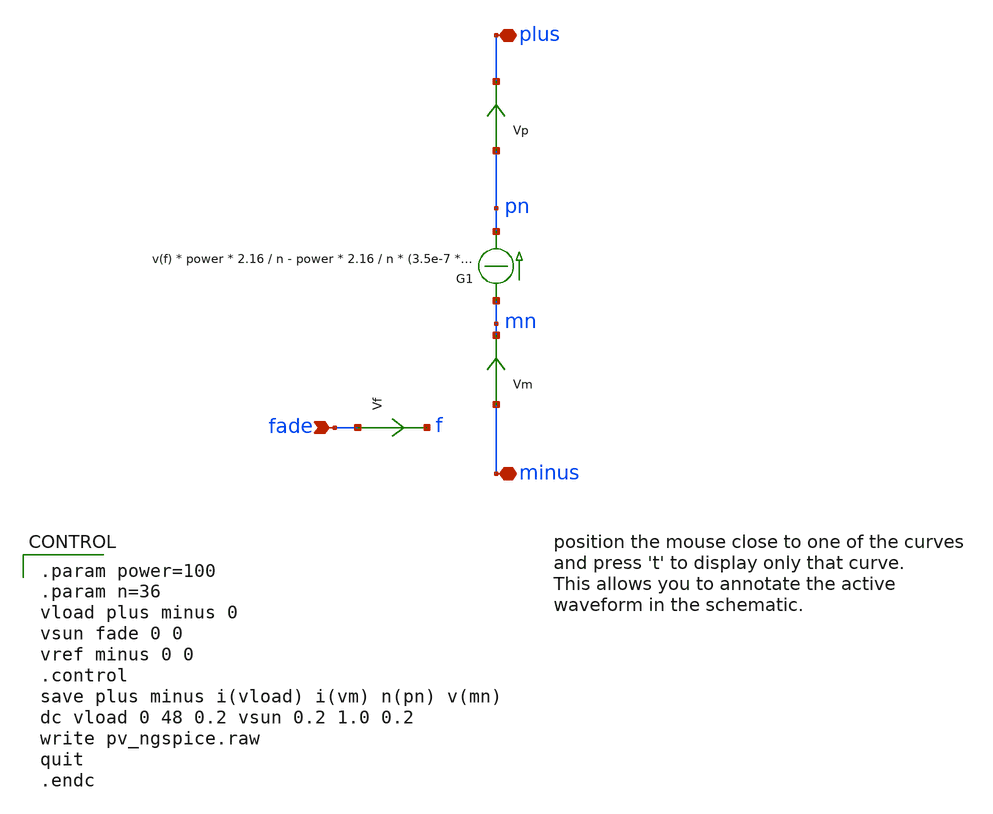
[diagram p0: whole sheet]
** sch_path: xschem_library/ngspice/pv_ngspice.sch
* Copyright (C) 1998-2023 Stefan Frederik Schippers
* This program is free software; you can redistribute it and/or modify
* it under the terms of the GNU General Public License as published by
* the Free Software Foundation; either version 2 of the License, or
* (at your option) any later version.
* This program is distributed in the hope that it will be useful,
* but WITHOUT ANY WARRANTY; without even the implied warranty of
* MERCHANTABILITY or FITNESS FOR A PARTICULAR PURPOSE.  See the
* GNU General Public License for more details.
* You should have received a copy of the GNU General Public License
* along with this program; if not, write to the Free Software
**.subckt pv_ngspice plus minus fade
*.iopin plus
*.iopin minus
*.ipin fade
Vm minus mn 0
.save i(vm)
G1 mn pn CUR=' v(f) * power * 2.16 / n - power * 2.16 / n * (3.5e-7 * exp( v(pn,mn) / n / 0.041)) '
Vf fade f 0
.save i(vf)
Vp pn plus 0
.save i(vp)
**** begin user architecture code

.param power=100
.param n=36
vload plus minus 0
vsun fade 0 0
vref minus 0 0
.control
save plus minus i(vload) i(vm) n(pn) v(mn)
dc vload 0 48 0.2 vsun 0.2 1.0 0.2
write pv_ngspice.raw
quit
.endc


**** end user architecture code
**.ends
.end
